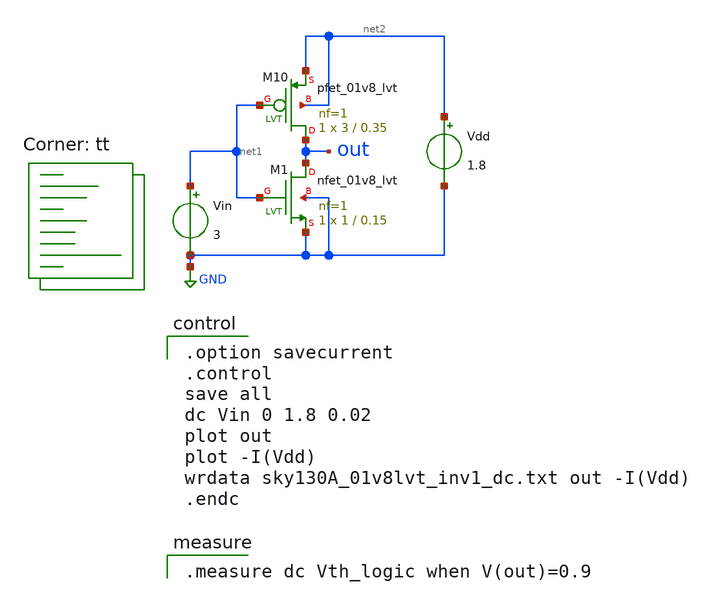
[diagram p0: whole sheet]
** sch_path: xschem/Logic/sky130A_01v8lvt_inv1_dc.sch
* Copyright 2021 Stefan Frederik Schippers
* Licensed under the Apache License, Version 2.0 (the "License");
* you may not use this file except in compliance with the License.
* You may obtain a copy of the License at
* https://www.apache.org/licenses/LICENSE-2.0
* Unless required by applicable law or agreed to in writing, software
* distributed under the License is distributed on an "AS IS" BASIS,
* WITHOUT WARRANTIES OR CONDITIONS OF ANY KIND, either express or implied.
* See the License for the specific language governing permissions and
* limitations under the License.
**.subckt sky130A_01v8lvt_inv1_dc
Vin net1 GND 3
Vdd net2 GND 1.8
XM1 out net1 GND GND sky130_fd_pr__nfet_01v8_lvt L=0.15 W=1 nf=1 ad='int((1 + 1)/2) * 1 / 1 * 0.29' as='int((1 + 2)/2) * 1 / 1 * 0.29'
+ pd='2*int((1 + 1)/2) * (1 / 1 + 0.29)' ps='2*int((1 + 2)/2) * (1 / 1 + 0.29)' nrd='0.29 / 1 ' nrs='0.29 / 1 '
+ sa=0 sb=0 sd=0 mult=1 m=1
XM10 out net1 net2 net2 sky130_fd_pr__pfet_01v8_lvt L=0.35 W=3 nf=1 ad='int((1 + 1)/2) * 3 / 1 * 0.29'
+ as='int((1 + 2)/2) * 3 / 1 * 0.29' pd='2*int((1 + 1)/2) * (3 / 1 + 0.29)' ps='2*int((1 + 2)/2) * (3 / 1 + 0.29)'
+ nrd='0.29 / 3 ' nrs='0.29 / 3 ' sa=0 sb=0 sd=0 mult=1 m=1
**** begin user architecture code
.lib $::SKYWATER_MODELS/sky130.lib.spice tt

.option savecurrent
.control
save all
dc Vin 0 1.8 0.02
plot out
plot -I(Vdd)
wrdata sky130A_01v8lvt_inv1_dc.txt out -I(Vdd)
.endc


.measure dc Vth_logic when V(out)=0.9

**** end user architecture code
**.ends
.GLOBAL GND
.end
